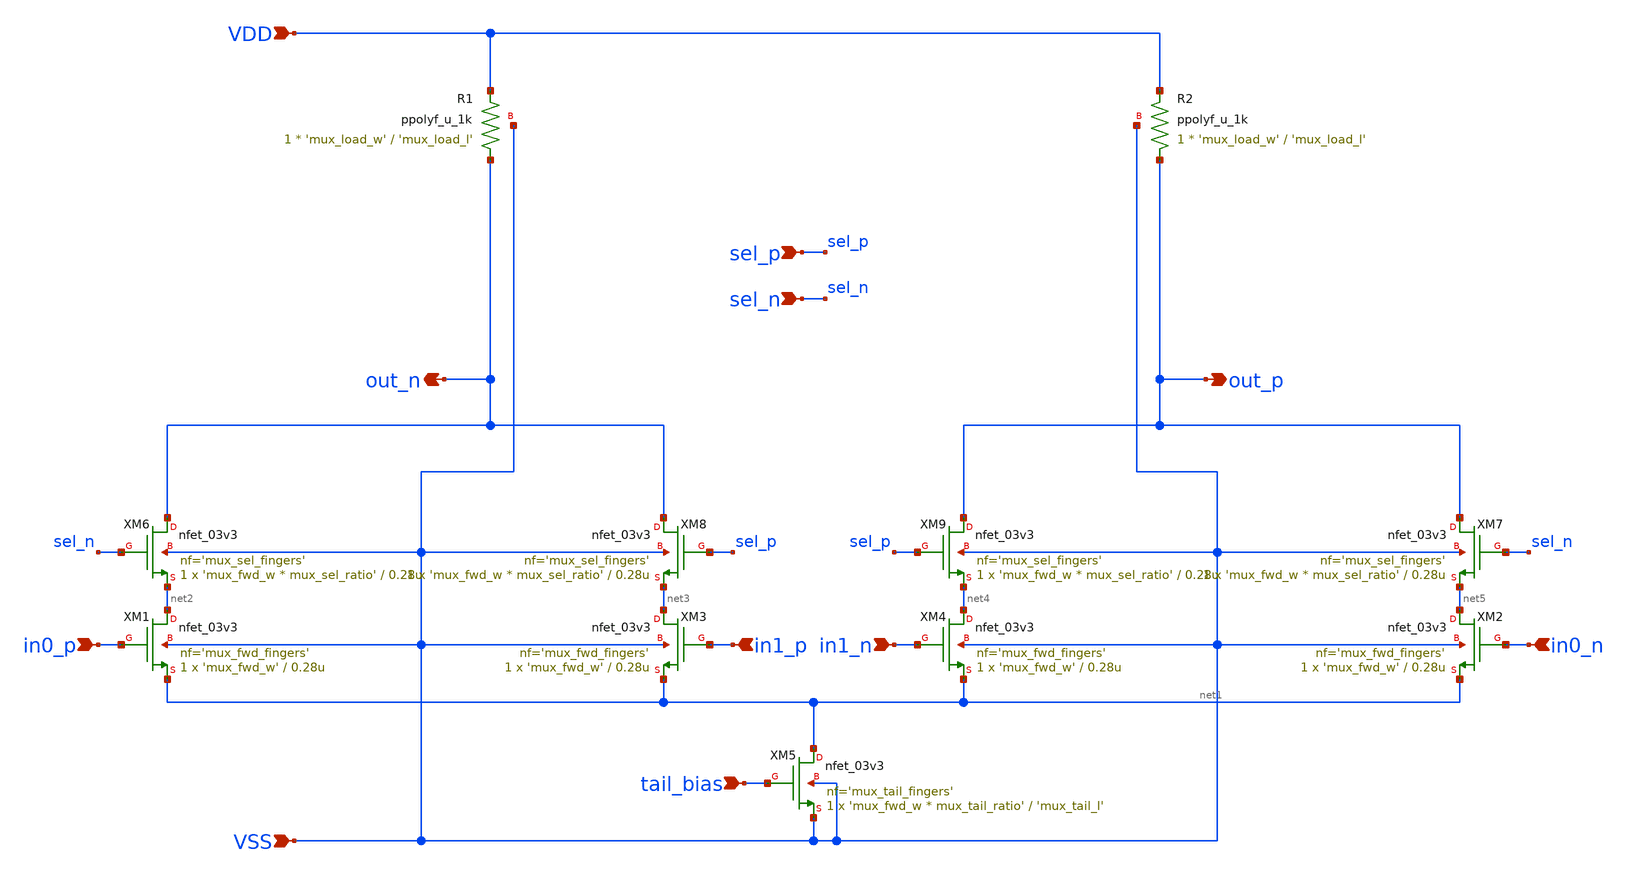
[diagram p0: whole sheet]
** sch_path: xschem/mux2_bottom_up.sch
**.subckt mux2_bottom_up VSS VDD out_n out_p in0_p in0_n sel_p sel_n tail_bias in1_p in1_n
*.ipin VSS
*.ipin VDD
*.opin out_n
*.opin out_p
*.ipin in0_p
*.ipin in0_n
*.ipin sel_p
*.ipin sel_n
*.ipin tail_bias
*.ipin in1_p
*.ipin in1_n
XM1 net2 in0_p net1 VSS nfet_03v3 L=0.28u W='mux_fwd_w' nf='mux_fwd_fingers' ad='int((nf+1)/2) * W/nf * 0.18u'
+ as='int((nf+2)/2) * W/nf * 0.18u' pd='2*int((nf+1)/2) * (W/nf + 0.18u)' ps='2*int((nf+2)/2) * (W/nf + 0.18u)'
+ nrd='0.18u / W' nrs='0.18u / W' sa=0 sb=0 sd=0 m=1
XM5 net1 tail_bias VSS VSS nfet_03v3 L='mux_tail_l' W='mux_fwd_w * mux_tail_ratio' nf='mux_tail_fingers'
+ ad='int((nf+1)/2) * W/nf * 0.18u' as='int((nf+2)/2) * W/nf * 0.18u' pd='2*int((nf+1)/2) * (W/nf + 0.18u)'
+ ps='2*int((nf+2)/2) * (W/nf + 0.18u)' nrd='0.18u / W' nrs='0.18u / W' sa=0 sb=0 sd=0 m=1
XM2 net5 in0_n net1 VSS nfet_03v3 L=0.28u W='mux_fwd_w' nf='mux_fwd_fingers' ad='int((nf+1)/2) * W/nf * 0.18u'
+ as='int((nf+2)/2) * W/nf * 0.18u' pd='2*int((nf+1)/2) * (W/nf + 0.18u)' ps='2*int((nf+2)/2) * (W/nf + 0.18u)'
+ nrd='0.18u / W' nrs='0.18u / W' sa=0 sb=0 sd=0 m=1
XR1 out_n VDD VSS ppolyf_u_1k r_width='mux_load_w' r_length='mux_load_l' m=1
XR2 out_p VDD VSS ppolyf_u_1k r_width='mux_load_w' r_length='mux_load_l' m=1
XM6 out_n sel_n net2 VSS nfet_03v3 L=0.28u W='mux_fwd_w * mux_sel_ratio' nf='mux_sel_fingers' ad='int((nf+1)/2) * W/nf * 0.18u'
+ as='int((nf+2)/2) * W/nf * 0.18u' pd='2*int((nf+1)/2) * (W/nf + 0.18u)' ps='2*int((nf+2)/2) * (W/nf + 0.18u)'
+ nrd='0.18u / W' nrs='0.18u / W' sa=0 sb=0 sd=0 m=1
XM7 out_p sel_n net5 VSS nfet_03v3 L=0.28u W='mux_fwd_w * mux_sel_ratio' nf='mux_sel_fingers' ad='int((nf+1)/2) * W/nf * 0.18u'
+ as='int((nf+2)/2) * W/nf * 0.18u' pd='2*int((nf+1)/2) * (W/nf + 0.18u)' ps='2*int((nf+2)/2) * (W/nf + 0.18u)'
+ nrd='0.18u / W' nrs='0.18u / W' sa=0 sb=0 sd=0 m=1
XM3 net3 in1_p net1 VSS nfet_03v3 L=0.28u W='mux_fwd_w' nf='mux_fwd_fingers' ad='int((nf+1)/2) * W/nf * 0.18u'
+ as='int((nf+2)/2) * W/nf * 0.18u' pd='2*int((nf+1)/2) * (W/nf + 0.18u)' ps='2*int((nf+2)/2) * (W/nf + 0.18u)'
+ nrd='0.18u / W' nrs='0.18u / W' sa=0 sb=0 sd=0 m=1
XM4 net4 in1_n net1 VSS nfet_03v3 L=0.28u W='mux_fwd_w' nf='mux_fwd_fingers' ad='int((nf+1)/2) * W/nf * 0.18u'
+ as='int((nf+2)/2) * W/nf * 0.18u' pd='2*int((nf+1)/2) * (W/nf + 0.18u)' ps='2*int((nf+2)/2) * (W/nf + 0.18u)'
+ nrd='0.18u / W' nrs='0.18u / W' sa=0 sb=0 sd=0 m=1
XM8 out_n sel_p net3 VSS nfet_03v3 L=0.28u W='mux_fwd_w * mux_sel_ratio' nf='mux_sel_fingers' ad='int((nf+1)/2) * W/nf * 0.18u'
+ as='int((nf+2)/2) * W/nf * 0.18u' pd='2*int((nf+1)/2) * (W/nf + 0.18u)' ps='2*int((nf+2)/2) * (W/nf + 0.18u)'
+ nrd='0.18u / W' nrs='0.18u / W' sa=0 sb=0 sd=0 m=1
XM9 out_p sel_p net4 VSS nfet_03v3 L=0.28u W='mux_fwd_w * mux_sel_ratio' nf='mux_sel_fingers' ad='int((nf+1)/2) * W/nf * 0.18u'
+ as='int((nf+2)/2) * W/nf * 0.18u' pd='2*int((nf+1)/2) * (W/nf + 0.18u)' ps='2*int((nf+2)/2) * (W/nf + 0.18u)'
+ nrd='0.18u / W' nrs='0.18u / W' sa=0 sb=0 sd=0 m=1
**.ends
.end
